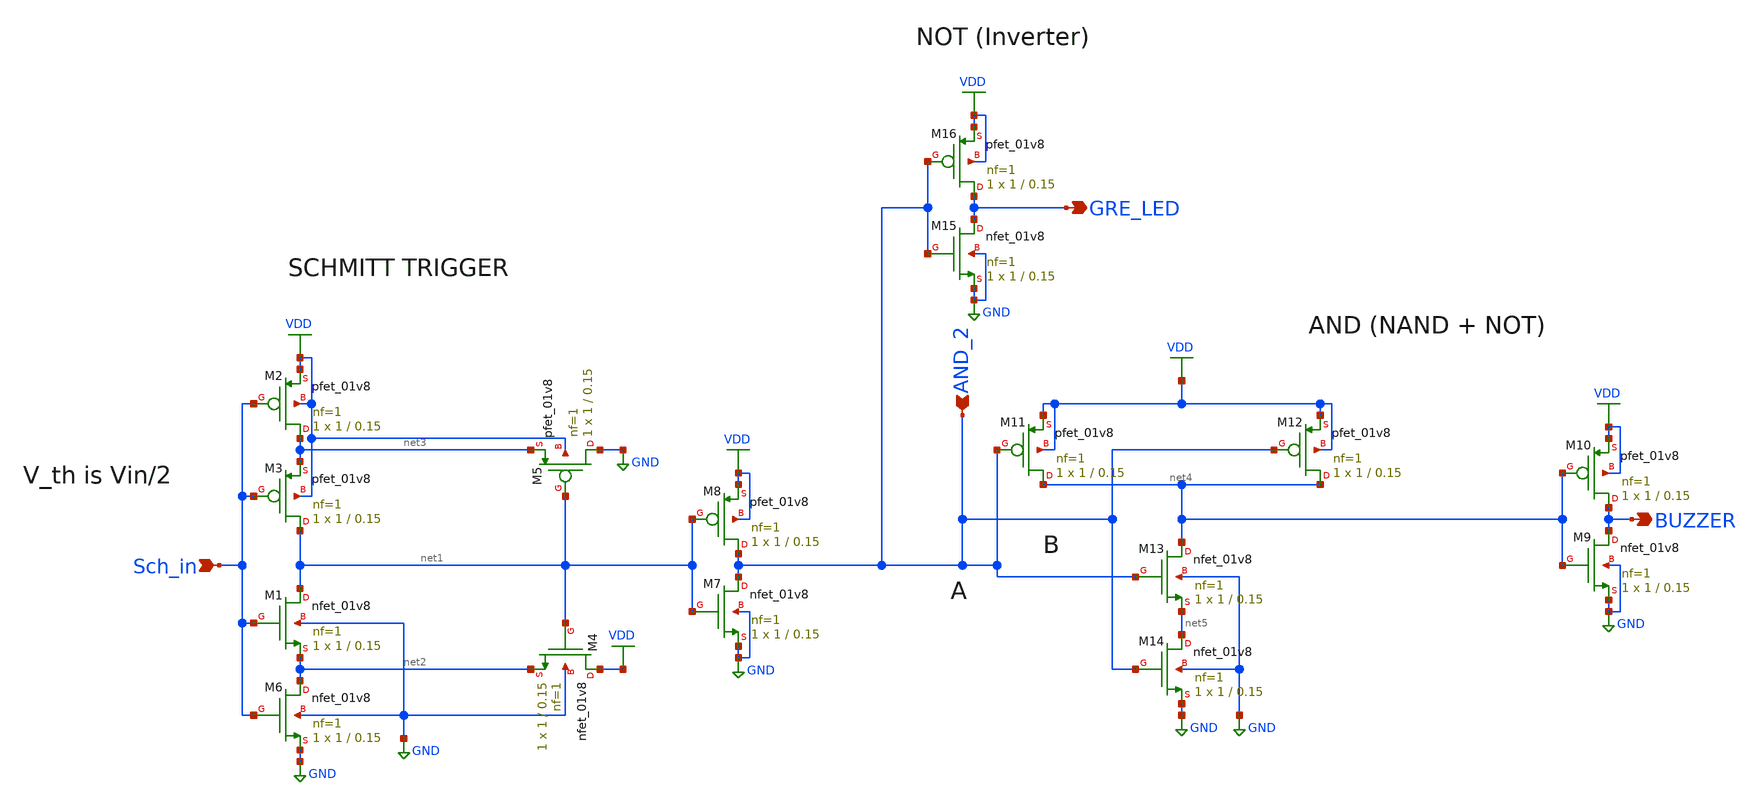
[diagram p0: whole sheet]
** sch_path: Schematic/detector_bomb_ASIC.sch
**.subckt detector_bomb_ASIC AND_2 GRE_LED Sch_in BUZZER
*.ipin AND_2
*.opin GRE_LED
*.ipin Sch_in
*.opin BUZZER
XM1 net1 Sch_in net2 GND sky130_fd_pr__nfet_01v8 L=0.15 W=1 nf=1 ad='int((1 + 1)/2) * 1 / 1 * 0.29' as='int((1 + 2)/2) * 1 / 1 * 0.29'
+ pd='2*int((1 + 1)/2) * (1 / 1 + 0.29)' ps='2*int((1 + 2)/2) * (1 / 1 + 0.29)' nrd='0.29 / 1 ' nrs='0.29 / 1 '
+ sa=0 sb=0 sd=0 mult=1 m=1
XM2 net3 Sch_in VDD VDD sky130_fd_pr__pfet_01v8 L=0.15 W=1 nf=1 ad='int((1 + 1)/2) * 1 / 1 * 0.29' as='int((1 + 2)/2) * 1 / 1 * 0.29'
+ pd='2*int((1 + 1)/2) * (1 / 1 + 0.29)' ps='2*int((1 + 2)/2) * (1 / 1 + 0.29)' nrd='0.29 / 1 ' nrs='0.29 / 1 '
+ sa=0 sb=0 sd=0 mult=1 m=1
XM3 net1 Sch_in net3 VDD sky130_fd_pr__pfet_01v8 L=0.15 W=1 nf=1 ad='int((1 + 1)/2) * 1 / 1 * 0.29' as='int((1 + 2)/2) * 1 / 1 * 0.29'
+ pd='2*int((1 + 1)/2) * (1 / 1 + 0.29)' ps='2*int((1 + 2)/2) * (1 / 1 + 0.29)' nrd='0.29 / 1 ' nrs='0.29 / 1 '
+ sa=0 sb=0 sd=0 mult=1 m=1
XM4 VDD net1 net2 GND sky130_fd_pr__nfet_01v8 L=0.15 W=1 nf=1 ad='int((1 + 1)/2) * 1 / 1 * 0.29' as='int((1 + 2)/2) * 1 / 1 * 0.29'
+ pd='2*int((1 + 1)/2) * (1 / 1 + 0.29)' ps='2*int((1 + 2)/2) * (1 / 1 + 0.29)' nrd='0.29 / 1 ' nrs='0.29 / 1 '
+ sa=0 sb=0 sd=0 mult=1 m=1
XM5 GND net1 net3 VDD sky130_fd_pr__pfet_01v8 L=0.15 W=1 nf=1 ad='int((1 + 1)/2) * 1 / 1 * 0.29' as='int((1 + 2)/2) * 1 / 1 * 0.29'
+ pd='2*int((1 + 1)/2) * (1 / 1 + 0.29)' ps='2*int((1 + 2)/2) * (1 / 1 + 0.29)' nrd='0.29 / 1 ' nrs='0.29 / 1 '
+ sa=0 sb=0 sd=0 mult=1 m=1
XM6 net2 Sch_in GND GND sky130_fd_pr__nfet_01v8 L=0.15 W=1 nf=1 ad='int((1 + 1)/2) * 1 / 1 * 0.29' as='int((1 + 2)/2) * 1 / 1 * 0.29'
+ pd='2*int((1 + 1)/2) * (1 / 1 + 0.29)' ps='2*int((1 + 2)/2) * (1 / 1 + 0.29)' nrd='0.29 / 1 ' nrs='0.29 / 1 '
+ sa=0 sb=0 sd=0 mult=1 m=1
XM7 AND_2 net1 GND GND sky130_fd_pr__nfet_01v8 L=0.15 W=1 nf=1 ad='int((1 + 1)/2) * 1 / 1 * 0.29' as='int((1 + 2)/2) * 1 / 1 * 0.29'
+ pd='2*int((1 + 1)/2) * (1 / 1 + 0.29)' ps='2*int((1 + 2)/2) * (1 / 1 + 0.29)' nrd='0.29 / 1 ' nrs='0.29 / 1 '
+ sa=0 sb=0 sd=0 mult=1 m=1
XM8 AND_2 net1 VDD VDD sky130_fd_pr__pfet_01v8 L=0.15 W=1 nf=1 ad='int((1 + 1)/2) * 1 / 1 * 0.29' as='int((1 + 2)/2) * 1 / 1 * 0.29'
+ pd='2*int((1 + 1)/2) * (1 / 1 + 0.29)' ps='2*int((1 + 2)/2) * (1 / 1 + 0.29)' nrd='0.29 / 1 ' nrs='0.29 / 1 '
+ sa=0 sb=0 sd=0 mult=1 m=1
XM9 BUZZER net4 GND GND sky130_fd_pr__nfet_01v8 L=0.15 W=1 nf=1 ad='int((1 + 1)/2) * 1 / 1 * 0.29' as='int((1 + 2)/2) * 1 / 1 * 0.29'
+ pd='2*int((1 + 1)/2) * (1 / 1 + 0.29)' ps='2*int((1 + 2)/2) * (1 / 1 + 0.29)' nrd='0.29 / 1 ' nrs='0.29 / 1 '
+ sa=0 sb=0 sd=0 mult=1 m=1
XM10 BUZZER net4 VDD VDD sky130_fd_pr__pfet_01v8 L=0.15 W=1 nf=1 ad='int((1 + 1)/2) * 1 / 1 * 0.29' as='int((1 + 2)/2) * 1 / 1 * 0.29'
+ pd='2*int((1 + 1)/2) * (1 / 1 + 0.29)' ps='2*int((1 + 2)/2) * (1 / 1 + 0.29)' nrd='0.29 / 1 ' nrs='0.29 / 1 '
+ sa=0 sb=0 sd=0 mult=1 m=1
XM11 net4 AND_2 VDD VDD sky130_fd_pr__pfet_01v8 L=0.15 W=1 nf=1 ad='int((1 + 1)/2) * 1 / 1 * 0.29' as='int((1 + 2)/2) * 1 / 1 * 0.29'
+ pd='2*int((1 + 1)/2) * (1 / 1 + 0.29)' ps='2*int((1 + 2)/2) * (1 / 1 + 0.29)' nrd='0.29 / 1 ' nrs='0.29 / 1 '
+ sa=0 sb=0 sd=0 mult=1 m=1
XM12 net4 AND_2 VDD VDD sky130_fd_pr__pfet_01v8 L=0.15 W=1 nf=1 ad='int((1 + 1)/2) * 1 / 1 * 0.29' as='int((1 + 2)/2) * 1 / 1 * 0.29'
+ pd='2*int((1 + 1)/2) * (1 / 1 + 0.29)' ps='2*int((1 + 2)/2) * (1 / 1 + 0.29)' nrd='0.29 / 1 ' nrs='0.29 / 1 '
+ sa=0 sb=0 sd=0 mult=1 m=1
XM13 net4 AND_2 net5 GND sky130_fd_pr__nfet_01v8 L=0.15 W=1 nf=1 ad='int((1 + 1)/2) * 1 / 1 * 0.29' as='int((1 + 2)/2) * 1 / 1 * 0.29'
+ pd='2*int((1 + 1)/2) * (1 / 1 + 0.29)' ps='2*int((1 + 2)/2) * (1 / 1 + 0.29)' nrd='0.29 / 1 ' nrs='0.29 / 1 '
+ sa=0 sb=0 sd=0 mult=1 m=1
XM14 net5 AND_2 GND GND sky130_fd_pr__nfet_01v8 L=0.15 W=1 nf=1 ad='int((1 + 1)/2) * 1 / 1 * 0.29' as='int((1 + 2)/2) * 1 / 1 * 0.29'
+ pd='2*int((1 + 1)/2) * (1 / 1 + 0.29)' ps='2*int((1 + 2)/2) * (1 / 1 + 0.29)' nrd='0.29 / 1 ' nrs='0.29 / 1 '
+ sa=0 sb=0 sd=0 mult=1 m=1
XM15 GRE_LED AND_2 GND GND sky130_fd_pr__nfet_01v8 L=0.15 W=1 nf=1 ad='int((1 + 1)/2) * 1 / 1 * 0.29'
+ as='int((1 + 2)/2) * 1 / 1 * 0.29' pd='2*int((1 + 1)/2) * (1 / 1 + 0.29)' ps='2*int((1 + 2)/2) * (1 / 1 + 0.29)'
+ nrd='0.29 / 1 ' nrs='0.29 / 1 ' sa=0 sb=0 sd=0 mult=1 m=1
XM16 GRE_LED AND_2 VDD VDD sky130_fd_pr__pfet_01v8 L=0.15 W=1 nf=1 ad='int((1 + 1)/2) * 1 / 1 * 0.29'
+ as='int((1 + 2)/2) * 1 / 1 * 0.29' pd='2*int((1 + 1)/2) * (1 / 1 + 0.29)' ps='2*int((1 + 2)/2) * (1 / 1 + 0.29)'
+ nrd='0.29 / 1 ' nrs='0.29 / 1 ' sa=0 sb=0 sd=0 mult=1 m=1
**.ends
.GLOBAL GND
.GLOBAL VDD
.end
